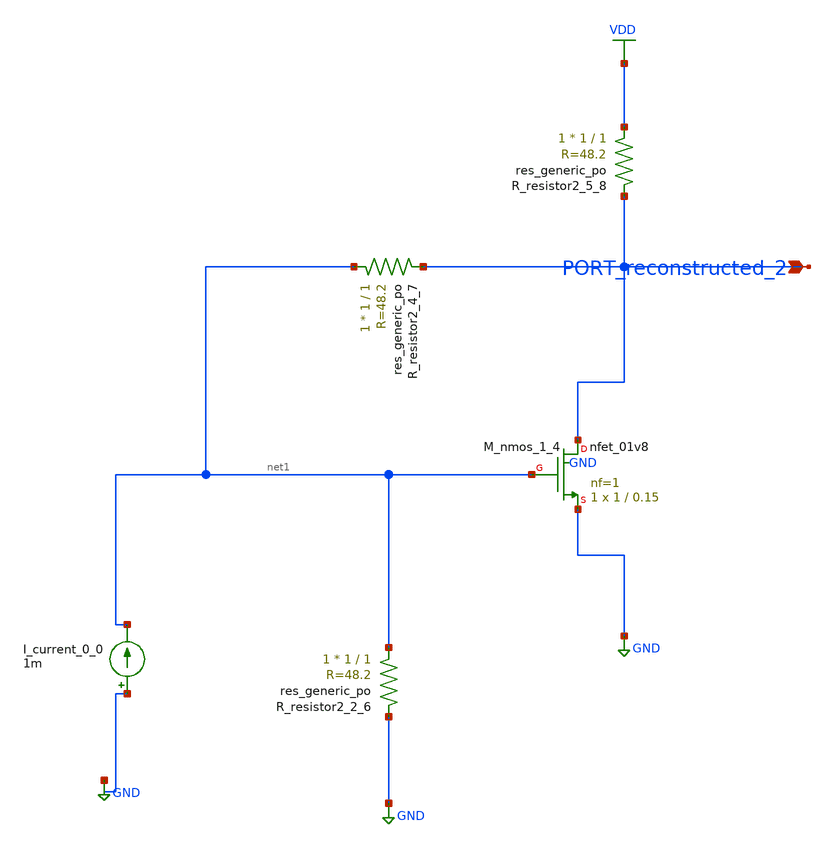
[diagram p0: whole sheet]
** sch_path: schematics/AMSNet/581.sch
**.subckt 581 PORT_reconstructed_2
*.ipin PORT_reconstructed_2
I_current_0_0 GND net1 1m
XM_nmos_1_4 PORT_reconstructed_2 net1 GND GND sky130_fd_pr__nfet_01v8 L=0.15 W=1 nf=1 ad='int((1 + 1)/2) * 1 / 1 * 0.29'
+ as='int((1 + 2)/2) * 1 / 1 * 0.29' pd='2*int((1 + 1)/2) * (1 / 1 + 0.29)' ps='2*int((1 + 2)/2) * (1 / 1 + 0.29)'
+ nrd='0.29 / 1 ' nrs='0.29 / 1 ' sa=0 sb=0 sd=0 mult=1 m=1
XR_resistor2_2_6 net1 GND sky130_fd_pr__res_generic_po W=1 L=1 m=1
XR_resistor2_4_7 net1 PORT_reconstructed_2 sky130_fd_pr__res_generic_po W=1 L=1 m=1
XR_resistor2_5_8 VDD PORT_reconstructed_2 sky130_fd_pr__res_generic_po W=1 L=1 m=1
**.ends
.GLOBAL GND
.GLOBAL VDD
.end
